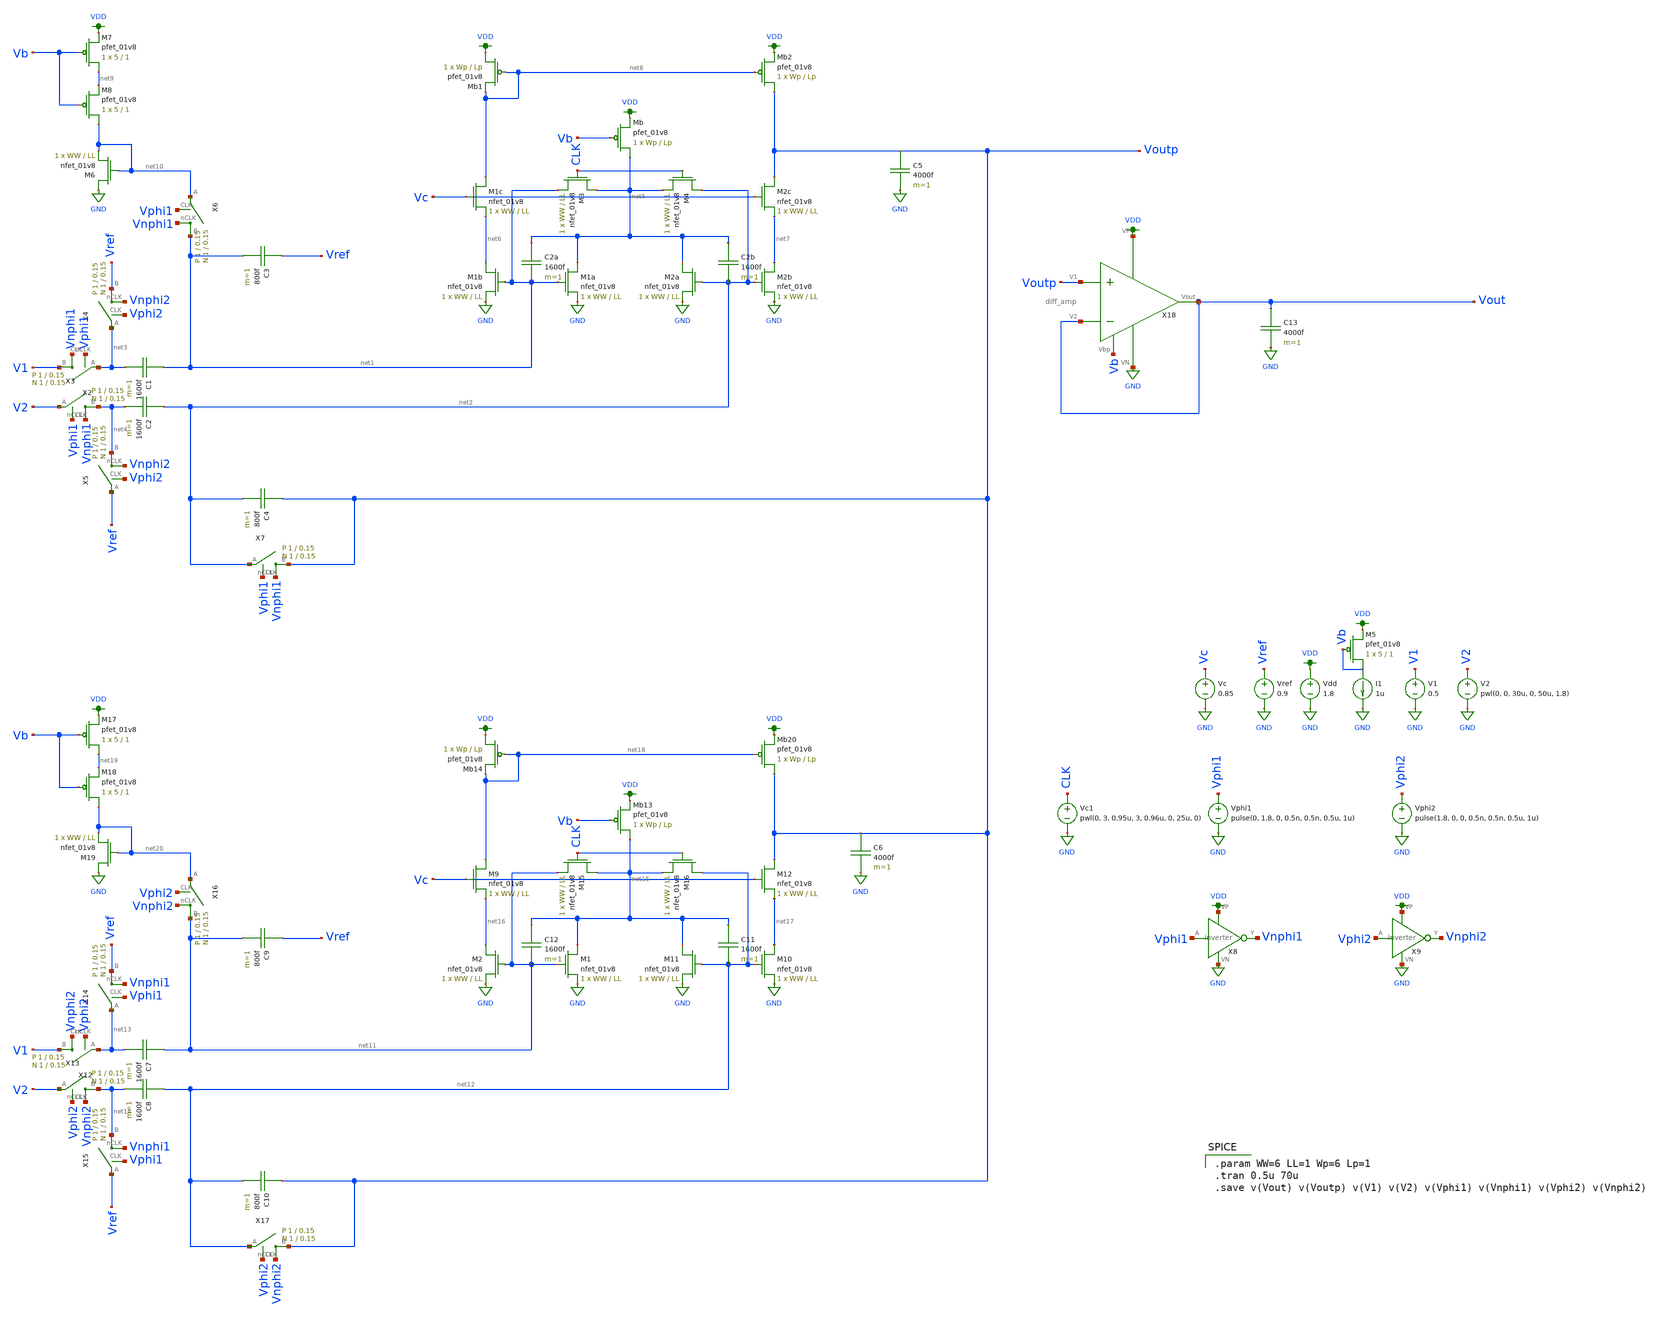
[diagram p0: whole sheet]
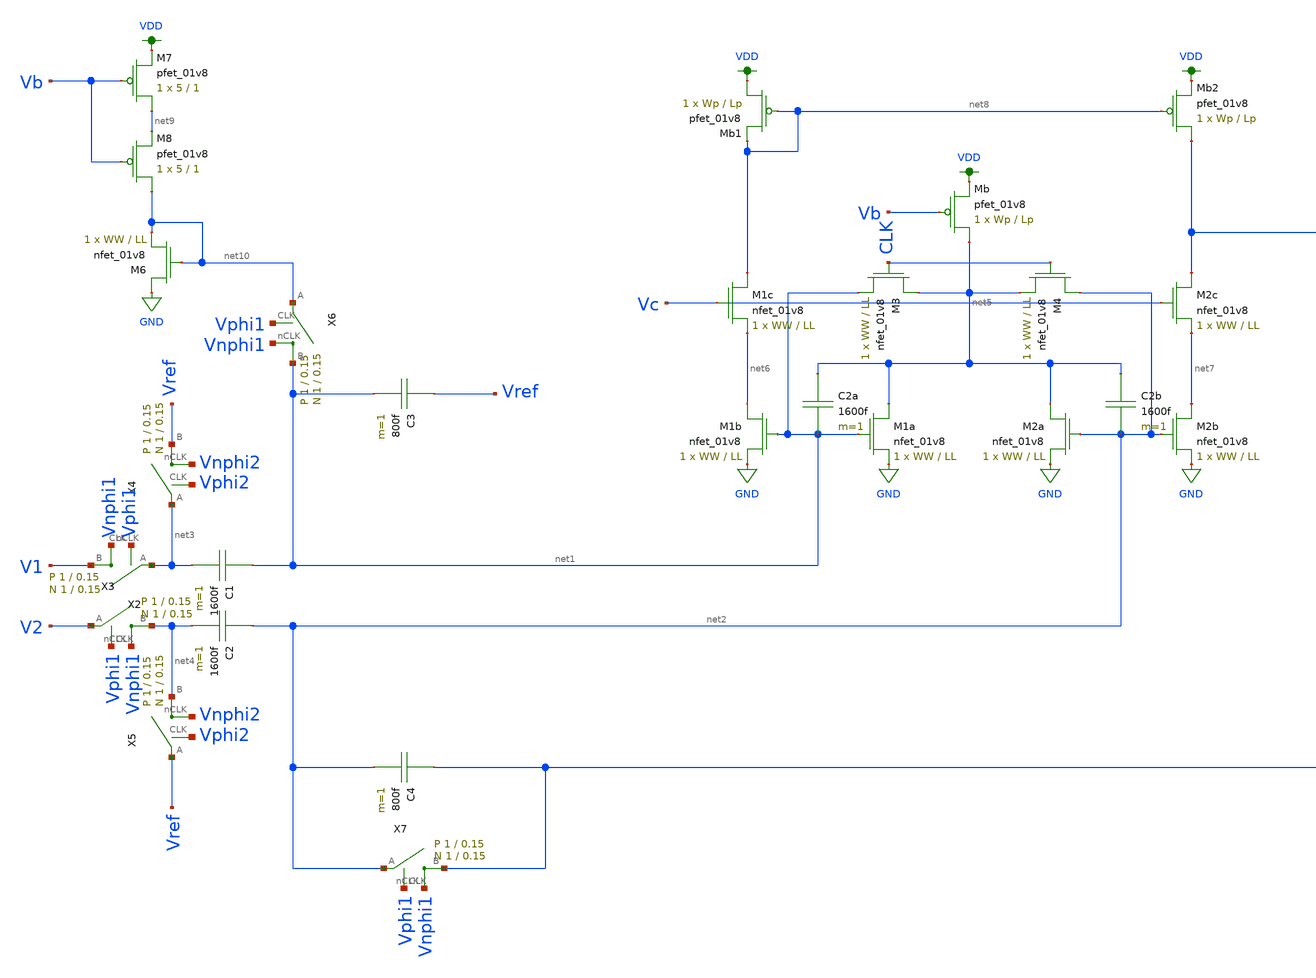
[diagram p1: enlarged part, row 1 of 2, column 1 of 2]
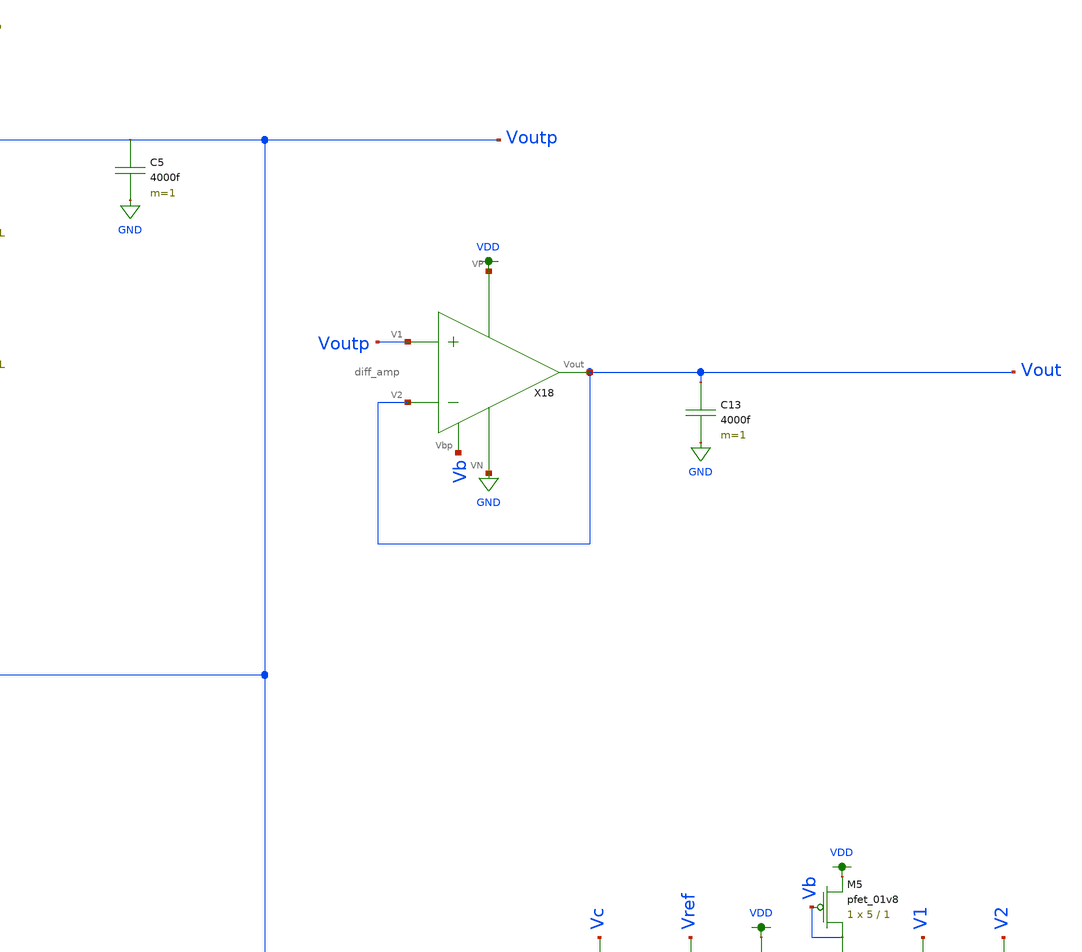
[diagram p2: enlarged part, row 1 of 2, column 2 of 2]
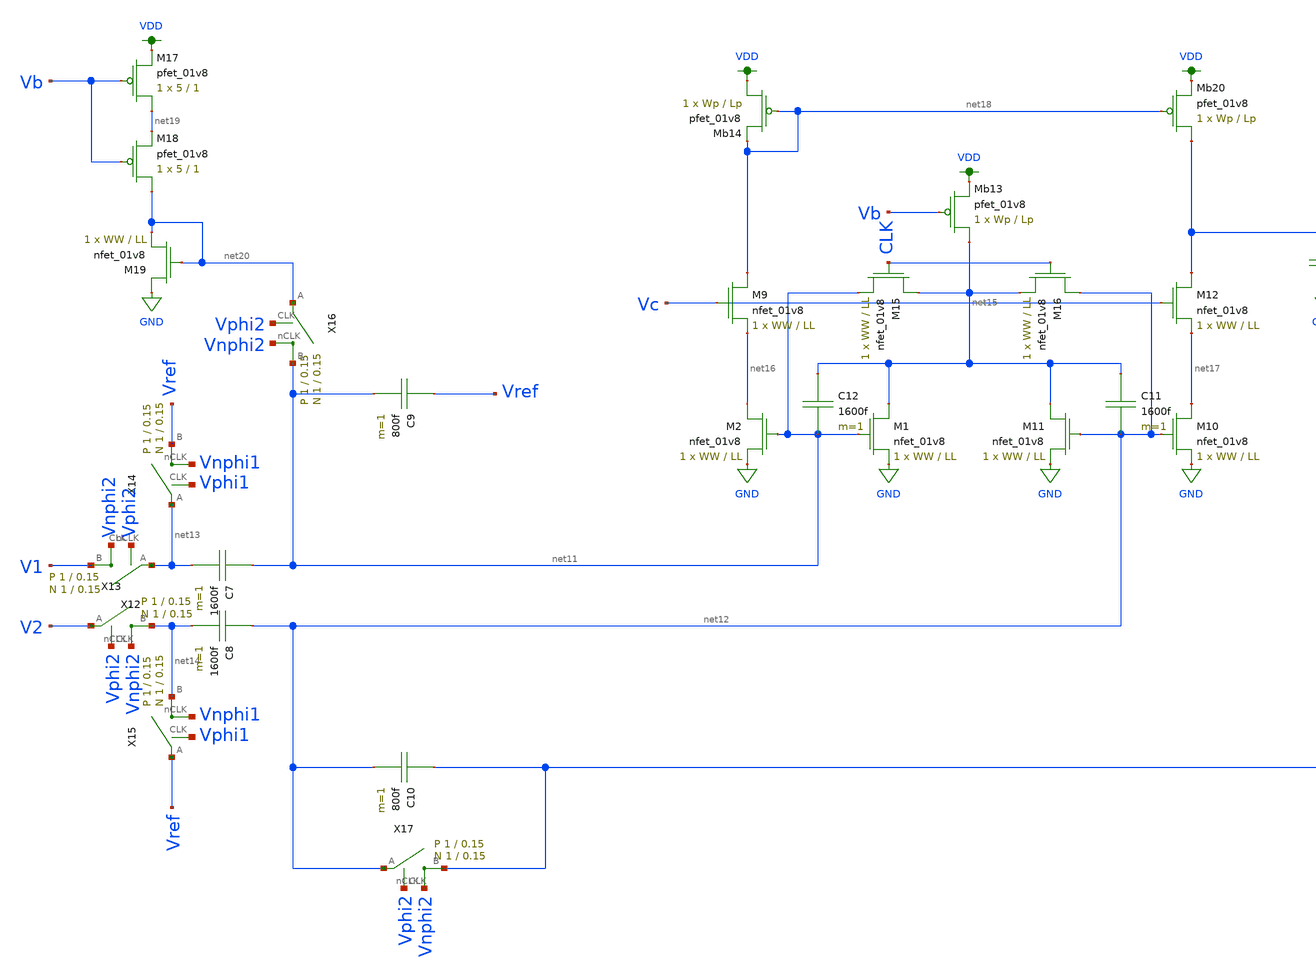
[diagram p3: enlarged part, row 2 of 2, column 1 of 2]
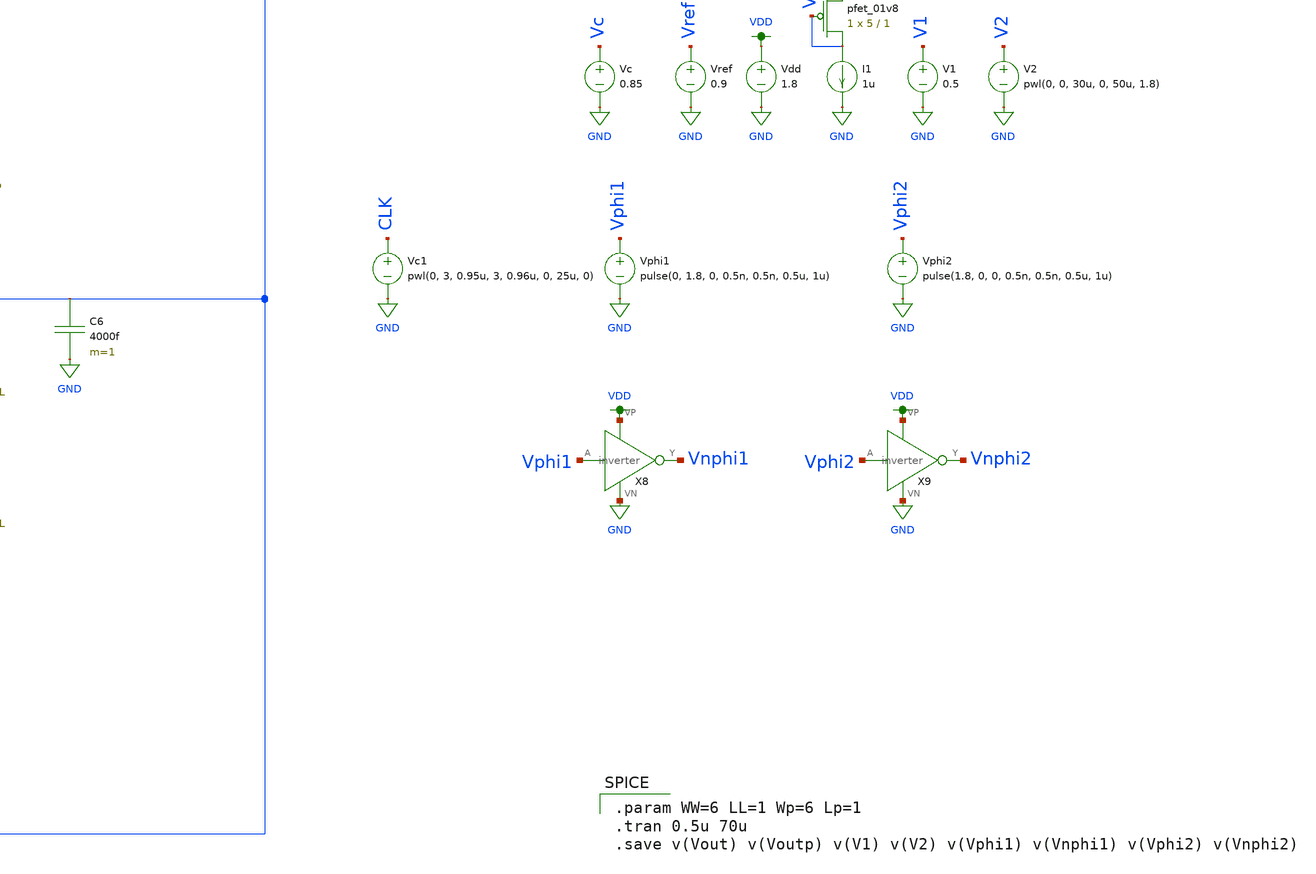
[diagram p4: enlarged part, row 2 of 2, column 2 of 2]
** sch_path: schematic/alpha_amp_ping_pong.sch
**.subckt alpha_amp_ping_pong
C1 net1 net3 1600f m=1
C2 net2 net4 1600f m=1
C3 Vref net1 800f m=1
C4 Voutp net2 800f m=1
X2 V1 net3 Vphi1 Vnphi1 switch Wp=1 Lp=0.15 WW=1 LL=0.15
X3 net4 V2 Vphi1 Vnphi1 switch Wp=1 Lp=0.15 WW=1 LL=0.15
X4 Vref net3 Vphi2 Vnphi2 switch Wp=1 Lp=0.15 WW=1 LL=0.15
X5 net4 Vref Vphi2 Vnphi2 switch Wp=1 Lp=0.15 WW=1 LL=0.15
X6 net1 net10 Vphi1 Vnphi1 switch Wp=1 Lp=0.15 WW=1 LL=0.15
X7 Voutp net2 Vphi1 Vnphi1 switch Wp=1 Lp=0.15 WW=1 LL=0.15
Vdd VDD GND 1.8
V1 V1 GND 0.5
V2 V2 GND pwl(0, 0, 30u, 0, 50u, 1.8)
Vphi1 Vphi1 GND pulse(0, 1.8, 0, 0.5n, 0.5n, 0.5u, 1u)
X8 Vphi1 Vnphi1 VDD GND inverter
Vphi2 Vphi2 GND pulse(1.8, 0, 0, 0.5n, 0.5n, 0.5u, 1u)
X9 Vphi2 Vnphi2 VDD GND inverter
Vref Vref GND 0.9
XM1a net5 net1 GND GND sky130_fd_pr__nfet_01v8 L=LL W=WW nf=1 ad='int((nf+1)/2) * W/nf * 0.29' as='int((nf+2)/2) * W/nf * 0.29'
+ pd='2*int((nf+1)/2) * (W/nf + 0.29)' ps='2*int((nf+2)/2) * (W/nf + 0.29)' nrd='0.29 / W' nrs='0.29 / W'
+ sa=0 sb=0 sd=0 mult=1 m=1
XM1b net6 net1 GND GND sky130_fd_pr__nfet_01v8 L=LL W=WW nf=1 ad='int((nf+1)/2) * W/nf * 0.29' as='int((nf+2)/2) * W/nf * 0.29'
+ pd='2*int((nf+1)/2) * (W/nf + 0.29)' ps='2*int((nf+2)/2) * (W/nf + 0.29)' nrd='0.29 / W' nrs='0.29 / W'
+ sa=0 sb=0 sd=0 mult=1 m=1
XM1c net8 Vc net6 GND sky130_fd_pr__nfet_01v8 L=LL W=WW nf=1 ad='int((nf+1)/2) * W/nf * 0.29' as='int((nf+2)/2) * W/nf * 0.29'
+ pd='2*int((nf+1)/2) * (W/nf + 0.29)' ps='2*int((nf+2)/2) * (W/nf + 0.29)' nrd='0.29 / W' nrs='0.29 / W'
+ sa=0 sb=0 sd=0 mult=1 m=1
XM2b net7 net2 GND GND sky130_fd_pr__nfet_01v8 L=LL W=WW nf=1 ad='int((nf+1)/2) * W/nf * 0.29' as='int((nf+2)/2) * W/nf * 0.29'
+ pd='2*int((nf+1)/2) * (W/nf + 0.29)' ps='2*int((nf+2)/2) * (W/nf + 0.29)' nrd='0.29 / W' nrs='0.29 / W'
+ sa=0 sb=0 sd=0 mult=1 m=1
XM2a net5 net2 GND GND sky130_fd_pr__nfet_01v8 L=LL W=WW nf=1 ad='int((nf+1)/2) * W/nf * 0.29' as='int((nf+2)/2) * W/nf * 0.29'
+ pd='2*int((nf+1)/2) * (W/nf + 0.29)' ps='2*int((nf+2)/2) * (W/nf + 0.29)' nrd='0.29 / W' nrs='0.29 / W'
+ sa=0 sb=0 sd=0 mult=1 m=1
XM2c Voutp Vc net7 GND sky130_fd_pr__nfet_01v8 L=LL W=WW nf=1 ad='int((nf+1)/2) * W/nf * 0.29' as='int((nf+2)/2) * W/nf * 0.29'
+ pd='2*int((nf+1)/2) * (W/nf + 0.29)' ps='2*int((nf+2)/2) * (W/nf + 0.29)' nrd='0.29 / W' nrs='0.29 / W'
+ sa=0 sb=0 sd=0 mult=1 m=1
XMb net5 Vb VDD VDD sky130_fd_pr__pfet_01v8 L=Lp W=Wp nf=1 ad='int((nf+1)/2) * W/nf * 0.29' as='int((nf+2)/2) * W/nf * 0.29'
+ pd='2*int((nf+1)/2) * (W/nf + 0.29)' ps='2*int((nf+2)/2) * (W/nf + 0.29)' nrd='0.29 / W' nrs='0.29 / W'
+ sa=0 sb=0 sd=0 mult=1 m=1
C2b net5 net2 1600f m=1
C2a net5 net1 1600f m=1
Vc Vc GND 0.85
XMb1 VDD net8 net8 VDD sky130_fd_pr__pfet_01v8 L=Lp W=Wp nf=1 ad='int((nf+1)/2) * W/nf * 0.29' as='int((nf+2)/2) * W/nf * 0.29'
+ pd='2*int((nf+1)/2) * (W/nf + 0.29)' ps='2*int((nf+2)/2) * (W/nf + 0.29)' nrd='0.29 / W' nrs='0.29 / W'
+ sa=0 sb=0 sd=0 mult=1 m=1
XM3 net5 CLK net1 GND sky130_fd_pr__nfet_01v8 L=LL W=WW nf=1 ad='int((nf+1)/2) * W/nf * 0.29' as='int((nf+2)/2) * W/nf * 0.29'
+ pd='2*int((nf+1)/2) * (W/nf + 0.29)' ps='2*int((nf+2)/2) * (W/nf + 0.29)' nrd='0.29 / W' nrs='0.29 / W'
+ sa=0 sb=0 sd=0 mult=1 m=1
XM4 net2 CLK net5 GND sky130_fd_pr__nfet_01v8 L=LL W=WW nf=1 ad='int((nf+1)/2) * W/nf * 0.29' as='int((nf+2)/2) * W/nf * 0.29'
+ pd='2*int((nf+1)/2) * (W/nf + 0.29)' ps='2*int((nf+2)/2) * (W/nf + 0.29)' nrd='0.29 / W' nrs='0.29 / W'
+ sa=0 sb=0 sd=0 mult=1 m=1
Vc1 CLK GND pwl(0, 3, 0.95u, 3, 0.96u, 0, 25u, 0)
XM5 Vb Vb VDD VDD sky130_fd_pr__pfet_01v8 L=1 W=5 nf=1 ad='int((nf+1)/2) * W/nf * 0.29' as='int((nf+2)/2) * W/nf * 0.29'
+ pd='2*int((nf+1)/2) * (W/nf + 0.29)' ps='2*int((nf+2)/2) * (W/nf + 0.29)' nrd='0.29 / W' nrs='0.29 / W'
+ sa=0 sb=0 sd=0 mult=1 m=1
I1 Vb GND 1u
XM7 net9 Vb VDD VDD sky130_fd_pr__pfet_01v8 L=1 W=5 nf=1 ad='int((nf+1)/2) * W/nf * 0.29' as='int((nf+2)/2) * W/nf * 0.29'
+ pd='2*int((nf+1)/2) * (W/nf + 0.29)' ps='2*int((nf+2)/2) * (W/nf + 0.29)' nrd='0.29 / W' nrs='0.29 / W'
+ sa=0 sb=0 sd=0 mult=1 m=1
XM8 net10 Vb net9 VDD sky130_fd_pr__pfet_01v8 L=1 W=5 nf=1 ad='int((nf+1)/2) * W/nf * 0.29' as='int((nf+2)/2) * W/nf * 0.29'
+ pd='2*int((nf+1)/2) * (W/nf + 0.29)' ps='2*int((nf+2)/2) * (W/nf + 0.29)' nrd='0.29 / W' nrs='0.29 / W'
+ sa=0 sb=0 sd=0 mult=1 m=1
XM6 GND net10 net10 GND sky130_fd_pr__nfet_01v8 L=LL W=WW nf=1 ad='int((nf+1)/2) * W/nf * 0.29' as='int((nf+2)/2) * W/nf * 0.29'
+ pd='2*int((nf+1)/2) * (W/nf + 0.29)' ps='2*int((nf+2)/2) * (W/nf + 0.29)' nrd='0.29 / W' nrs='0.29 / W'
+ sa=0 sb=0 sd=0 mult=1 m=1
XMb2 Voutp net8 VDD VDD sky130_fd_pr__pfet_01v8 L=Lp W=Wp nf=1 ad='int((nf+1)/2) * W/nf * 0.29' as='int((nf+2)/2) * W/nf * 0.29'
+ pd='2*int((nf+1)/2) * (W/nf + 0.29)' ps='2*int((nf+2)/2) * (W/nf + 0.29)' nrd='0.29 / W' nrs='0.29 / W'
+ sa=0 sb=0 sd=0 mult=1 m=1
C7 net11 net13 1600f m=1
C8 net12 net14 1600f m=1
C9 Vref net11 800f m=1
C10 Voutp net12 800f m=1
X12 V1 net13 Vphi2 Vnphi2 switch Wp=1 Lp=0.15 WW=1 LL=0.15
X13 net14 V2 Vphi2 Vnphi2 switch Wp=1 Lp=0.15 WW=1 LL=0.15
X14 Vref net13 Vphi1 Vnphi1 switch Wp=1 Lp=0.15 WW=1 LL=0.15
X15 net14 Vref Vphi1 Vnphi1 switch Wp=1 Lp=0.15 WW=1 LL=0.15
X16 net11 net20 Vphi2 Vnphi2 switch Wp=1 Lp=0.15 WW=1 LL=0.15
X17 Voutp net12 Vphi2 Vnphi2 switch Wp=1 Lp=0.15 WW=1 LL=0.15
XM1 net15 net11 GND GND sky130_fd_pr__nfet_01v8 L=LL W=WW nf=1 ad='int((nf+1)/2) * W/nf * 0.29' as='int((nf+2)/2) * W/nf * 0.29'
+ pd='2*int((nf+1)/2) * (W/nf + 0.29)' ps='2*int((nf+2)/2) * (W/nf + 0.29)' nrd='0.29 / W' nrs='0.29 / W'
+ sa=0 sb=0 sd=0 mult=1 m=1
XM2 net16 net11 GND GND sky130_fd_pr__nfet_01v8 L=LL W=WW nf=1 ad='int((nf+1)/2) * W/nf * 0.29' as='int((nf+2)/2) * W/nf * 0.29'
+ pd='2*int((nf+1)/2) * (W/nf + 0.29)' ps='2*int((nf+2)/2) * (W/nf + 0.29)' nrd='0.29 / W' nrs='0.29 / W'
+ sa=0 sb=0 sd=0 mult=1 m=1
XM9 net18 Vc net16 GND sky130_fd_pr__nfet_01v8 L=LL W=WW nf=1 ad='int((nf+1)/2) * W/nf * 0.29' as='int((nf+2)/2) * W/nf * 0.29'
+ pd='2*int((nf+1)/2) * (W/nf + 0.29)' ps='2*int((nf+2)/2) * (W/nf + 0.29)' nrd='0.29 / W' nrs='0.29 / W'
+ sa=0 sb=0 sd=0 mult=1 m=1
XM10 net17 net12 GND GND sky130_fd_pr__nfet_01v8 L=LL W=WW nf=1 ad='int((nf+1)/2) * W/nf * 0.29' as='int((nf+2)/2) * W/nf * 0.29'
+ pd='2*int((nf+1)/2) * (W/nf + 0.29)' ps='2*int((nf+2)/2) * (W/nf + 0.29)' nrd='0.29 / W' nrs='0.29 / W'
+ sa=0 sb=0 sd=0 mult=1 m=1
XM11 net15 net12 GND GND sky130_fd_pr__nfet_01v8 L=LL W=WW nf=1 ad='int((nf+1)/2) * W/nf * 0.29' as='int((nf+2)/2) * W/nf * 0.29'
+ pd='2*int((nf+1)/2) * (W/nf + 0.29)' ps='2*int((nf+2)/2) * (W/nf + 0.29)' nrd='0.29 / W' nrs='0.29 / W'
+ sa=0 sb=0 sd=0 mult=1 m=1
XM12 Voutp Vc net17 GND sky130_fd_pr__nfet_01v8 L=LL W=WW nf=1 ad='int((nf+1)/2) * W/nf * 0.29' as='int((nf+2)/2) * W/nf * 0.29'
+ pd='2*int((nf+1)/2) * (W/nf + 0.29)' ps='2*int((nf+2)/2) * (W/nf + 0.29)' nrd='0.29 / W' nrs='0.29 / W'
+ sa=0 sb=0 sd=0 mult=1 m=1
XMb13 net15 Vb VDD VDD sky130_fd_pr__pfet_01v8 L=Lp W=Wp nf=1 ad='int((nf+1)/2) * W/nf * 0.29' as='int((nf+2)/2) * W/nf * 0.29'
+ pd='2*int((nf+1)/2) * (W/nf + 0.29)' ps='2*int((nf+2)/2) * (W/nf + 0.29)' nrd='0.29 / W' nrs='0.29 / W'
+ sa=0 sb=0 sd=0 mult=1 m=1
C11 net15 net12 1600f m=1
C12 net15 net11 1600f m=1
XMb14 VDD net18 net18 VDD sky130_fd_pr__pfet_01v8 L=Lp W=Wp nf=1 ad='int((nf+1)/2) * W/nf * 0.29' as='int((nf+2)/2) * W/nf * 0.29'
+ pd='2*int((nf+1)/2) * (W/nf + 0.29)' ps='2*int((nf+2)/2) * (W/nf + 0.29)' nrd='0.29 / W' nrs='0.29 / W'
+ sa=0 sb=0 sd=0 mult=1 m=1
XM15 net15 CLK net11 GND sky130_fd_pr__nfet_01v8 L=LL W=WW nf=1 ad='int((nf+1)/2) * W/nf * 0.29' as='int((nf+2)/2) * W/nf * 0.29'
+ pd='2*int((nf+1)/2) * (W/nf + 0.29)' ps='2*int((nf+2)/2) * (W/nf + 0.29)' nrd='0.29 / W' nrs='0.29 / W'
+ sa=0 sb=0 sd=0 mult=1 m=1
XM16 net12 CLK net15 GND sky130_fd_pr__nfet_01v8 L=LL W=WW nf=1 ad='int((nf+1)/2) * W/nf * 0.29' as='int((nf+2)/2) * W/nf * 0.29'
+ pd='2*int((nf+1)/2) * (W/nf + 0.29)' ps='2*int((nf+2)/2) * (W/nf + 0.29)' nrd='0.29 / W' nrs='0.29 / W'
+ sa=0 sb=0 sd=0 mult=1 m=1
XM17 net19 Vb VDD VDD sky130_fd_pr__pfet_01v8 L=1 W=5 nf=1 ad='int((nf+1)/2) * W/nf * 0.29' as='int((nf+2)/2) * W/nf * 0.29'
+ pd='2*int((nf+1)/2) * (W/nf + 0.29)' ps='2*int((nf+2)/2) * (W/nf + 0.29)' nrd='0.29 / W' nrs='0.29 / W'
+ sa=0 sb=0 sd=0 mult=1 m=1
XM18 net20 Vb net19 VDD sky130_fd_pr__pfet_01v8 L=1 W=5 nf=1 ad='int((nf+1)/2) * W/nf * 0.29' as='int((nf+2)/2) * W/nf * 0.29'
+ pd='2*int((nf+1)/2) * (W/nf + 0.29)' ps='2*int((nf+2)/2) * (W/nf + 0.29)' nrd='0.29 / W' nrs='0.29 / W'
+ sa=0 sb=0 sd=0 mult=1 m=1
XM19 GND net20 net20 GND sky130_fd_pr__nfet_01v8 L=LL W=WW nf=1 ad='int((nf+1)/2) * W/nf * 0.29' as='int((nf+2)/2) * W/nf * 0.29'
+ pd='2*int((nf+1)/2) * (W/nf + 0.29)' ps='2*int((nf+2)/2) * (W/nf + 0.29)' nrd='0.29 / W' nrs='0.29 / W'
+ sa=0 sb=0 sd=0 mult=1 m=1
XMb20 Voutp net18 VDD VDD sky130_fd_pr__pfet_01v8 L=Lp W=Wp nf=1 ad='int((nf+1)/2) * W/nf * 0.29' as='int((nf+2)/2) * W/nf * 0.29'
+ pd='2*int((nf+1)/2) * (W/nf + 0.29)' ps='2*int((nf+2)/2) * (W/nf + 0.29)' nrd='0.29 / W' nrs='0.29 / W'
+ sa=0 sb=0 sd=0 mult=1 m=1
X18 VDD Vb Vout Voutp Vout GND diff_amp
C13 Vout GND 4000f m=1
C5 Voutp GND 4000f m=1
C6 Voutp GND 4000f m=1
**** begin user architecture code

.option wnflag=1
.param MC_SWITCH=0.0
.lib ~/skywater/skywater-pdk/libraries/sky130_fd_pr_ngspice/latest/models/sky130.lib.spice tt


.param WW=6 LL=1 Wp=6 Lp=1
.tran 0.5u 70u
.save v(Vout) v(Voutp) v(V1) v(V2) v(Vphi1) v(Vnphi1) v(Vphi2) v(Vnphi2)

**** end user architecture code
**.ends
.GLOBAL GND
.GLOBAL VDD
.end
